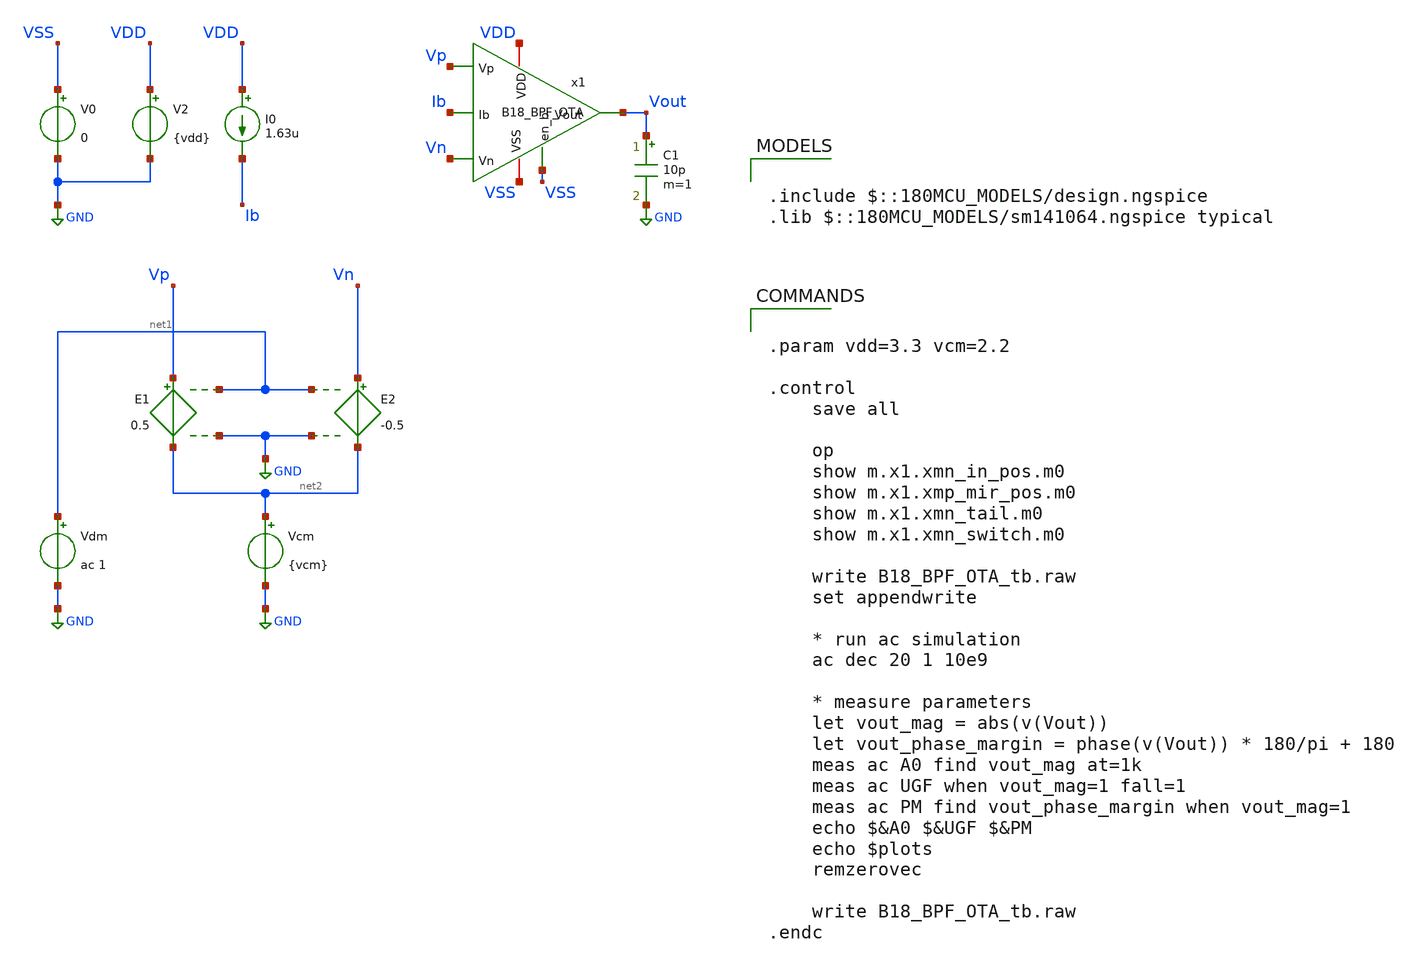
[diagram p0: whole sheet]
** sch_path: Analog/schematics/1_readout/bpf/B18_BPF_OTA_tb.sch
**.subckt B18_BPF_OTA_tb
I0 VDD Ib 1.63u
C1 Vout GND 10p m=1
V0 VSS GND 0
V2 VDD GND {vdd}
E1 Vp net2 net1 GND 0.5
E2 Vn net2 net1 GND -0.5
Vdm net1 GND ac 1
Vcm net2 GND {vcm}
x1 Vp Vn Vout VDD VSS Ib VSS B18_BPF_OTA
**** begin user architecture code


.param vdd=3.3 vcm=2.2

.control
    save all

    op
    show m.x1.xmn_in_pos.m0
    show m.x1.xmp_mir_pos.m0
    show m.x1.xmn_tail.m0
    show m.x1.xmn_switch.m0

    write B18_BPF_OTA_tb.raw
    set appendwrite

    * run ac simulation
    ac dec 20 1 10e9

    * measure parameters
    let vout_mag = abs(v(Vout))
    let vout_phase_margin = phase(v(Vout)) * 180/pi + 180
    meas ac A0 find vout_mag at=1k
    meas ac UGF when vout_mag=1 fall=1
    meas ac PM find vout_phase_margin when vout_mag=1
    echo $&A0 $&UGF $&PM
    echo $plots
    remzerovec

    write B18_BPF_OTA_tb.raw
.endc



.include $::180MCU_MODELS/design.ngspice
.lib $::180MCU_MODELS/sm141064.ngspice typical



*ICMR is 3.3v to 1.24v, tested op with vcm = 2.2v


**** end user architecture code
**.ends

* expanding   symbol:  Analog/schematics/1_readout/bpf/B18_BPF_OTA.sym # of pins=7
** sym_path: Analog/schematics/1_readout/bpf/B18_BPF_OTA.sym
** sch_path: Analog/schematics/1_readout/bpf/B18_BPF_OTA.sch
.subckt B18_BPF_OTA Vp Vn Vout VDD VSS Ib en_b
*.ipin Vp
*.ipin Vn
*.opin Vout
*.iopin VDD
*.iopin VSS
*.ipin Ib
*.ipin en_b
XMP_MIR_NEG Vout net1 VDD VDD pfet_03v3 L=0.7u W=1.62u nf=1 ad='int((nf+1)/2) * W/nf * 0.18u' as='int((nf+2)/2) * W/nf * 0.18u'
+ pd='2*int((nf+1)/2) * (W/nf + 0.18u)' ps='2*int((nf+2)/2) * (W/nf + 0.18u)' nrd='0.18u / W' nrs='0.18u / W'
+ sa=0 sb=0 sd=0 m=1
XMP_MIR_POS net1 net1 VDD VDD pfet_03v3 L=0.7u W=1.62u nf=1 ad='int((nf+1)/2) * W/nf * 0.18u' as='int((nf+2)/2) * W/nf * 0.18u'
+ pd='2*int((nf+1)/2) * (W/nf + 0.18u)' ps='2*int((nf+2)/2) * (W/nf + 0.18u)' nrd='0.18u / W' nrs='0.18u / W'
+ sa=0 sb=0 sd=0 m=1
XMN_IN_POS net1 Vp net2 VSS nfet_03v3 L=0.7u W=0.42u nf=1 ad='int((nf+1)/2) * W/nf * 0.18u' as='int((nf+2)/2) * W/nf * 0.18u'
+ pd='2*int((nf+1)/2) * (W/nf + 0.18u)' ps='2*int((nf+2)/2) * (W/nf + 0.18u)' nrd='0.18u / W' nrs='0.18u / W'
+ sa=0 sb=0 sd=0 m=1
XMN_IN_NEG Vout Vn net2 VSS nfet_03v3 L=0.7u W=0.42u nf=1 ad='int((nf+1)/2) * W/nf * 0.18u' as='int((nf+2)/2) * W/nf * 0.18u'
+ pd='2*int((nf+1)/2) * (W/nf + 0.18u)' ps='2*int((nf+2)/2) * (W/nf + 0.18u)' nrd='0.18u / W' nrs='0.18u / W'
+ sa=0 sb=0 sd=0 m=1
XMN_TAIL net2 Ib VSS VSS nfet_03v3 L=0.7u W=0.83u nf=1 ad='int((nf+1)/2) * W/nf * 0.18u' as='int((nf+2)/2) * W/nf * 0.18u'
+ pd='2*int((nf+1)/2) * (W/nf + 0.18u)' ps='2*int((nf+2)/2) * (W/nf + 0.18u)' nrd='0.18u / W' nrs='0.18u / W'
+ sa=0 sb=0 sd=0 m=1
XMN_TAILMIR Ib Ib VSS VSS nfet_03v3 L=0.7u W=0.83u nf=1 ad='int((nf+1)/2) * W/nf * 0.18u' as='int((nf+2)/2) * W/nf * 0.18u'
+ pd='2*int((nf+1)/2) * (W/nf + 0.18u)' ps='2*int((nf+2)/2) * (W/nf + 0.18u)' nrd='0.18u / W' nrs='0.18u / W'
+ sa=0 sb=0 sd=0 m=1
XMN_SWITCH Ib en_b VSS VSS nfet_03v3 L=0.5u W=1u nf=1 ad='int((nf+1)/2) * W/nf * 0.18u' as='int((nf+2)/2) * W/nf * 0.18u'
+ pd='2*int((nf+1)/2) * (W/nf + 0.18u)' ps='2*int((nf+2)/2) * (W/nf + 0.18u)' nrd='0.18u / W' nrs='0.18u / W'
+ sa=0 sb=0 sd=0 m=1
.ends

.GLOBAL GND
.end
